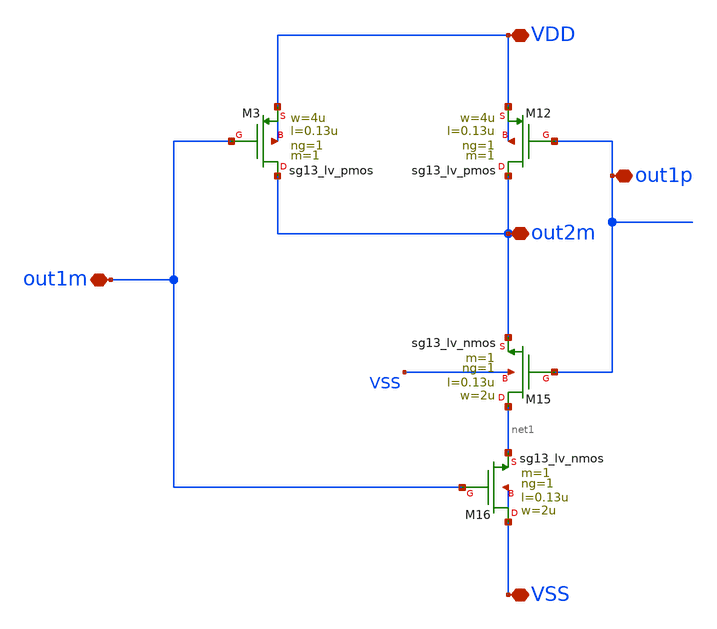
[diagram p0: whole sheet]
** sch_path: 5_Design/4_Layout/Team 5/xschem/comp_5_split2.sch
**.subckt comp_5_split2 out1m out2m out1p VSS VDD
*.iopin out1m
*.iopin out2m
*.iopin out1p
*.iopin VSS
*.iopin VDD
XM3 out2m out1m VDD VDD sg13_lv_pmos w=4u l=0.13u ng=1 m=1 mm_ok=1
XM12 out2m out1p VDD VDD sg13_lv_pmos w=4u l=0.13u ng=1 m=1 mm_ok=1
XM15 net1 out1p out2m VSS sg13_lv_nmos w=2u l=0.13u ng=1 m=1 mm_ok=1
XM16 VSS out1m net1 VSS sg13_lv_nmos w=2u l=0.13u ng=1 m=1 mm_ok=1
**.ends
.end
